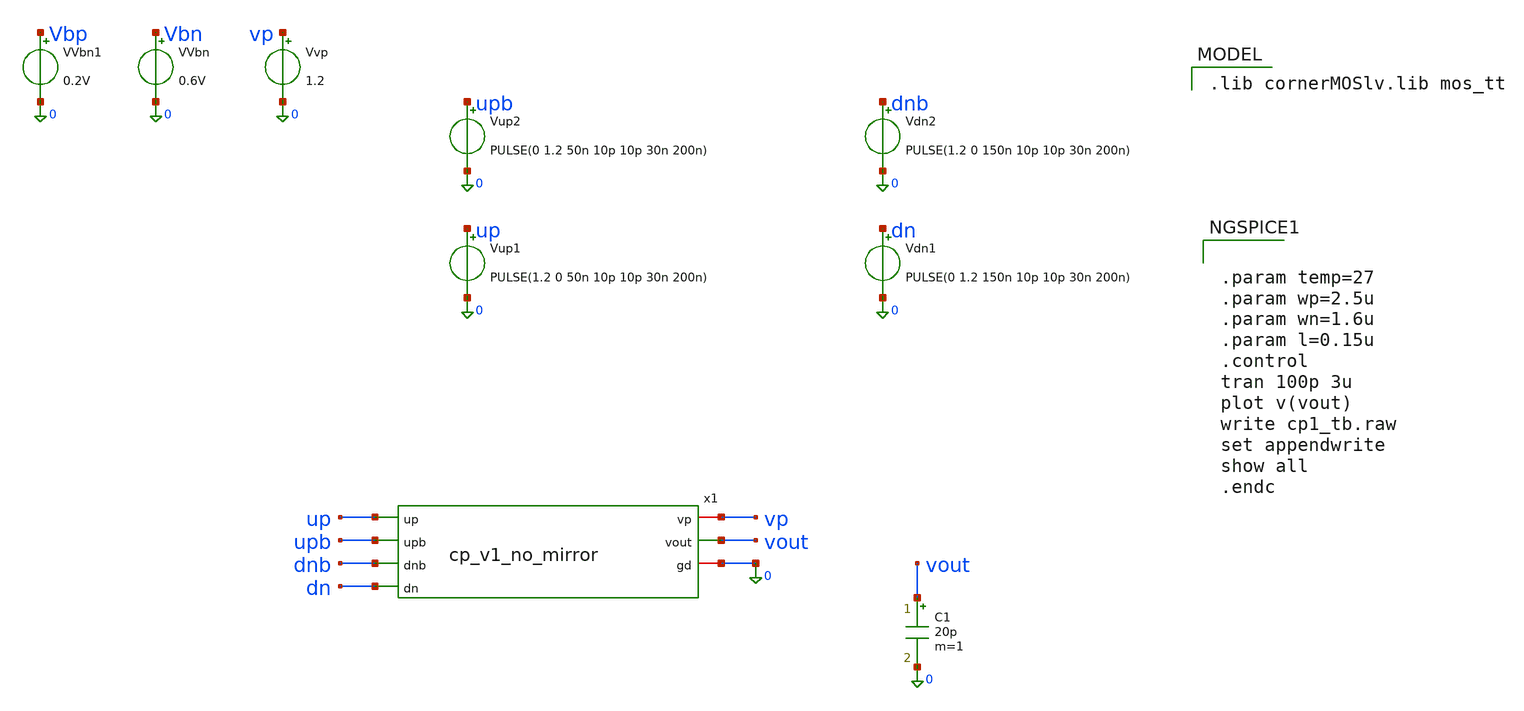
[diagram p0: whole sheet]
** sch_path: charge_pump/cp_v1_tb.sch
**.subckt cp_v1_tb
Vvp vp 0 1.2
VVbn Vbn 0 0.6V
Vup1 up 0 PULSE(1.2 0 50n 10p 10p 30n 200n)
Vdn1 dn 0 PULSE(0 1.2 150n 10p 10p 30n 200n)
C1 vout 0 20p m=1
Vup2 upb 0 PULSE(0 1.2 50n 10p 10p 30n 200n)
Vdn2 dnb 0 PULSE(1.2 0 150n 10p 10p 30n 200n)
VVbn1 Vbp 0 0.2V
x1 vp up upb vout dnb dn 0 cp_v1_no_mirror
**** begin user architecture code
 .lib cornerMOSlv.lib mos_tt



.param temp=27
.param wp=2.5u
.param wn=1.6u
.param l=0.15u
.control
tran 100p 3u
plot v(vout)
write cp1_tb.raw
set appendwrite
show all
.endc


**** end user architecture code
**.ends
.end
